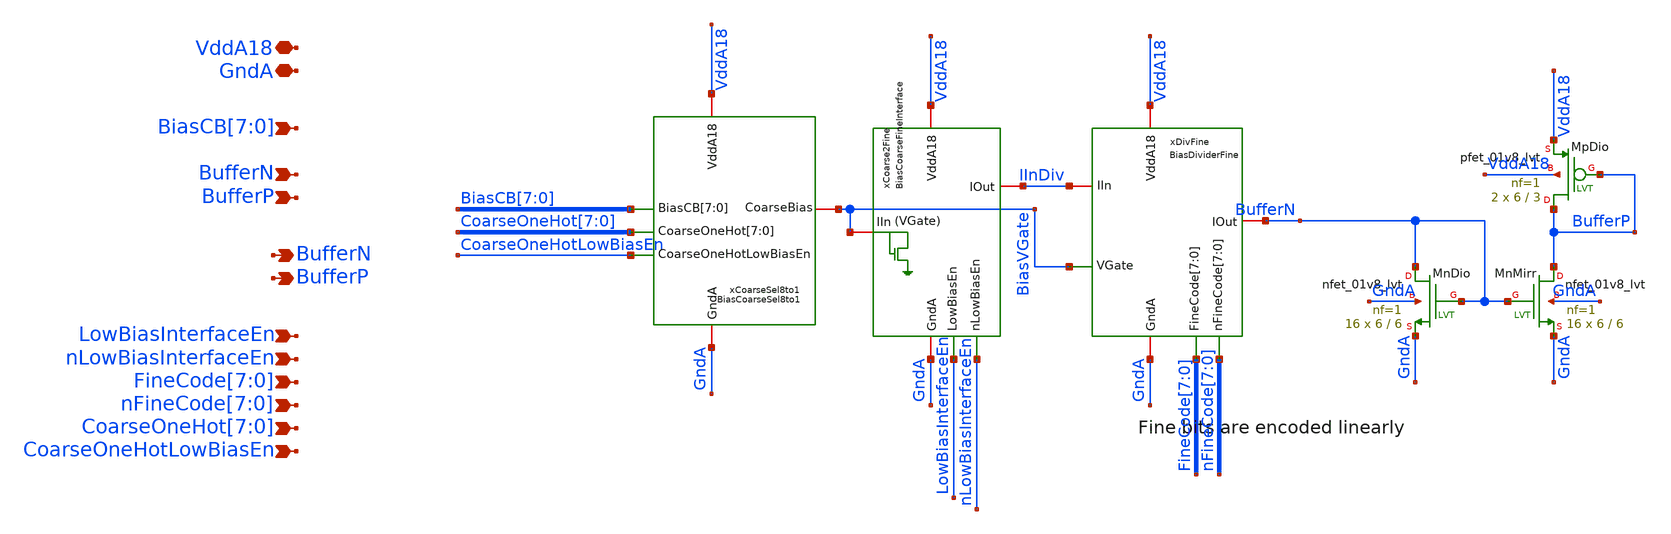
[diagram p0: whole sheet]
** sch_path: analog/klayout/production/final_merge_20260923/testbenches/cace/analog/xschem/BiasBranchBuffer.sch
**.subckt BiasBranchBuffer VddA18 GndA BufferN
*+ BiasCB[7],BiasCB[6],BiasCB[5],BiasCB[4],BiasCB[3],BiasCB[2],BiasCB[1],BiasCB[0] BufferN BufferP BufferP LowBiasInterfaceEn nLowBiasInterfaceEn
*+ FineCode[7],FineCode[6],FineCode[5],FineCode[4],FineCode[3],FineCode[2],FineCode[1],FineCode[0]
*+ nFineCode[7],nFineCode[6],nFineCode[5],nFineCode[4],nFineCode[3],nFineCode[2],nFineCode[1],nFineCode[0]
*+ CoarseOneHot[7],CoarseOneHot[6],CoarseOneHot[5],CoarseOneHot[4],CoarseOneHot[3],CoarseOneHot[2],CoarseOneHot[1],CoarseOneHot[0] CoarseOneHotLowBiasEn
*.iopin VddA18
*.iopin GndA
*.opin BufferN
*.ipin BiasCB[7],BiasCB[6],BiasCB[5],BiasCB[4],BiasCB[3],BiasCB[2],BiasCB[1],BiasCB[0]
*.ipin BufferN
*.ipin BufferP
*.opin BufferP
*.ipin LowBiasInterfaceEn
*.ipin nLowBiasInterfaceEn
*.ipin
*+ FineCode[7],FineCode[6],FineCode[5],FineCode[4],FineCode[3],FineCode[2],FineCode[1],FineCode[0]
*.ipin
*+ nFineCode[7],nFineCode[6],nFineCode[5],nFineCode[4],nFineCode[3],nFineCode[2],nFineCode[1],nFineCode[0]
*.ipin
*+ CoarseOneHot[7],CoarseOneHot[6],CoarseOneHot[5],CoarseOneHot[4],CoarseOneHot[3],CoarseOneHot[2],CoarseOneHot[1],CoarseOneHot[0]
*.ipin CoarseOneHotLowBiasEn
xCoarse2Fine VddA18 GndA LowBiasInterfaceEn nLowBiasInterfaceEn BiasVGate IInDiv
+ BiasCoarseFineInterface
xDivFine VddA18 GndA FineCode[7] FineCode[6] FineCode[5] FineCode[4] FineCode[3] FineCode[2]
+ FineCode[1] FineCode[0] nFineCode[7] nFineCode[6] nFineCode[5] nFineCode[4] nFineCode[3] nFineCode[2]
+ nFineCode[1] nFineCode[0] IInDiv BufferN BiasVGate BiasDividerFine
XMpDio BufferP BufferP VddA18 VddA18 sky130_fd_pr__pfet_01v8_lvt L=3 W=6 nf=1 ad='int((1 + 1)/2) * 6 / 1 * 0.29'
+ as='int((1 + 2)/2) * 6 / 1 * 0.29' pd='2*int((1 + 1)/2) * (6 / 1 + 0.29)' ps='2*int((1 + 2)/2) * (6 / 1 + 0.29)'
+ nrd='0.29 / 6 ' nrs='0.29 / 6 ' sa=0 sb=0 sd=0 mult=2 m=2
XMnDio BufferN BufferN GndA GndA sky130_fd_pr__nfet_01v8_lvt L=6 W=6 nf=1 ad='int((1 + 1)/2) * 6 / 1 * 0.29'
+ as='int((1 + 2)/2) * 6 / 1 * 0.29' pd='2*int((1 + 1)/2) * (6 / 1 + 0.29)' ps='2*int((1 + 2)/2) * (6 / 1 + 0.29)'
+ nrd='0.29 / 6 ' nrs='0.29 / 6 ' sa=0 sb=0 sd=0 mult=16 m=16
XMnMirr BufferP BufferN GndA GndA sky130_fd_pr__nfet_01v8_lvt L=6 W=6 nf=1 ad='int((1 + 1)/2) * 6 / 1 * 0.29'
+ as='int((1 + 2)/2) * 6 / 1 * 0.29' pd='2*int((1 + 1)/2) * (6 / 1 + 0.29)' ps='2*int((1 + 2)/2) * (6 / 1 + 0.29)'
+ nrd='0.29 / 6 ' nrs='0.29 / 6 ' sa=0 sb=0 sd=0 mult=16 m=16
xCoarseSel8to1 VddA18 GndA CoarseOneHot[7] CoarseOneHot[6] CoarseOneHot[5] CoarseOneHot[4]
+ CoarseOneHot[3] CoarseOneHot[2] CoarseOneHot[1] CoarseOneHot[0] CoarseOneHotLowBiasEn BiasCB[7] BiasCB[6] BiasCB[5]
+ BiasCB[4] BiasCB[3] BiasCB[2] BiasCB[1] BiasCB[0] BiasVGate BiasCoarseSel8to1
**.ends

* expanding   symbol:  BiasCoarseFineInterface.sym # of pins=6
** sym_path: analog/xschem/BiasCoarseFineInterface.sym
** sch_path: analog/xschem/BiasCoarseFineInterface.sch
.subckt BiasCoarseFineInterface VddA18 GndA LowBiasEn nLowBiasEn IIn IOut
*.iopin GndA
*.iopin VddA18
*.iopin IIn
*.iopin IOut
*.ipin nLowBiasEn
*.ipin LowBiasEn
XMpDisableHighBias HighBiasDioGate nLowBiasEn VddA18 VddA18 sky130_fd_pr__pfet_01v8 L=0.15 W=0.55 nf=1
+ ad='int((1 + 1)/2) * 0.55 / 1 * 0.29' as='int((1 + 2)/2) * 0.55 / 1 * 0.29' pd='2*int((1 + 1)/2) * (0.55 / 1 + 0.29)'
+ ps='2*int((1 + 2)/2) * (0.55 / 1 + 0.29)' nrd='0.29 / 0.55 ' nrs='0.29 / 0.55 ' sa=0 sb=0 sd=0 mult=1
+ m=1
XMpDioHighBias HighBiasDioDrain HighBiasDioGate VddA18 VddA18 sky130_fd_pr__pfet_01v8 L=0.5 W=64 nf=2
+ ad='int((2 + 1)/2) * 64 / 2 * 0.29' as='int((2 + 2)/2) * 64 / 2 * 0.29' pd='2*int((2 + 1)/2) * (64 / 2 + 0.29)'
+ ps='2*int((2 + 2)/2) * (64 / 2 + 0.29)' nrd='0.29 / 64 ' nrs='0.29 / 64 ' sa=0 sb=0 sd=0 mult=8 m=8
XMpMirrHighBias HighBiasMirr HighBiasDioGate VddA18 VddA18 sky130_fd_pr__pfet_01v8 L=0.5 W=64 nf=2 ad='int((2 + 1)/2) * 64 / 2 * 0.29'
+ as='int((2 + 2)/2) * 64 / 2 * 0.29' pd='2*int((2 + 1)/2) * (64 / 2 + 0.29)' ps='2*int((2 + 2)/2) * (64 / 2 + 0.29)'
+ nrd='0.29 / 64 ' nrs='0.29 / 64 ' sa=0 sb=0 sd=0 mult=8 m=8
XMpswDioHighBias HighBiasDioGate LowBiasEn HighBiasDioDrain VddA18 sky130_fd_pr__pfet_01v8 L=0.5 W=0.55
+ nf=1 ad='int((1 + 1)/2) * 0.55 / 1 * 0.29' as='int((1 + 2)/2) * 0.55 / 1 * 0.29' pd='2*int((1 + 1)/2) * (0.55 / 1 + 0.29)'
+ ps='2*int((1 + 2)/2) * (0.55 / 1 + 0.29)' nrd='0.29 / 0.55 ' nrs='0.29 / 0.55 ' sa=0 sb=0 sd=0 mult=1
+ m=1
XMnDisableDioHighBias HighBiasDioDrain LowBiasEn GndA GndA sky130_fd_pr__nfet_01v8 L=0.15 W=0.42 nf=1
+ ad='int((1 + 1)/2) * 0.42 / 1 * 0.29' as='int((1 + 2)/2) * 0.42 / 1 * 0.29' pd='2*int((1 + 1)/2) * (0.42 / 1 + 0.29)'
+ ps='2*int((1 + 2)/2) * (0.42 / 1 + 0.29)' nrd='0.29 / 0.42 ' nrs='0.29 / 0.42 ' sa=0 sb=0 sd=0 mult=1
+ m=1
XMpSelDioHighBias net1 LowBiasEn HighBiasDioDrain VddA18 sky130_fd_pr__pfet_01v8_hvt L=0.5 W=32 nf=2
+ ad='int((2 + 1)/2) * 32 / 2 * 0.29' as='int((2 + 2)/2) * 32 / 2 * 0.29' pd='2*int((2 + 1)/2) * (32 / 2 + 0.29)'
+ ps='2*int((2 + 2)/2) * (32 / 2 + 0.29)' nrd='0.29 / 32 ' nrs='0.29 / 32 ' sa=0 sb=0 sd=0 mult=8 m=8
XMpSelMirrHighBias IOut LowBiasEn HighBiasMirr VddA18 sky130_fd_pr__pfet_01v8_hvt L=0.5 W=32 nf=2 ad='int((2 + 1)/2) * 32 / 2 * 0.29'
+ as='int((2 + 2)/2) * 32 / 2 * 0.29' pd='2*int((2 + 1)/2) * (32 / 2 + 0.29)' ps='2*int((2 + 2)/2) * (32 / 2 + 0.29)'
+ nrd='0.29 / 32 ' nrs='0.29 / 32 ' sa=0 sb=0 sd=0 mult=8 m=8
XMnDisableOutMirr HighBiasMirr LowBiasEn GndA GndA sky130_fd_pr__nfet_01v8 L=0.15 W=0.42 nf=1 ad='int((1 + 1)/2) * 0.42 / 1 * 0.29'
+ as='int((1 + 2)/2) * 0.42 / 1 * 0.29' pd='2*int((1 + 1)/2) * (0.42 / 1 + 0.29)' ps='2*int((1 + 2)/2) * (0.42 / 1 + 0.29)'
+ nrd='0.29 / 0.42 ' nrs='0.29 / 0.42 ' sa=0 sb=0 sd=0 mult=1 m=1
XMpInDio IIn IIn net1 VddA18 sky130_fd_pr__pfet_01v8_lvt L=1 W=9 nf=1 ad='int((1 + 1)/2) * 9 / 1 * 0.29'
+ as='int((1 + 2)/2) * 9 / 1 * 0.29' pd='2*int((1 + 1)/2) * (9 / 1 + 0.29)' ps='2*int((1 + 2)/2) * (9 / 1 + 0.29)'
+ nrd='0.29 / 9 ' nrs='0.29 / 9 ' sa=0 sb=0 sd=0 mult=2 m=2
XMpDioLowBias1 LowBiasDioInt LowBiasDioGate VddA18 VddA18 sky130_fd_pr__pfet_01v8 L=2 W=4 nf=1 ad='int((1 + 1)/2) * 4 / 1 * 0.29'
+ as='int((1 + 2)/2) * 4 / 1 * 0.29' pd='2*int((1 + 1)/2) * (4 / 1 + 0.29)' ps='2*int((1 + 2)/2) * (4 / 1 + 0.29)'
+ nrd='0.29 / 4 ' nrs='0.29 / 4 ' sa=0 sb=0 sd=0 mult=2 m=2
XMpMirrLowBias1 LowBiasMirrInt LowBiasDioGate VddA18 VddA18 sky130_fd_pr__pfet_01v8 L=2 W=4 nf=1 ad='int((1 + 1)/2) * 4 / 1 * 0.29'
+ as='int((1 + 2)/2) * 4 / 1 * 0.29' pd='2*int((1 + 1)/2) * (4 / 1 + 0.29)' ps='2*int((1 + 2)/2) * (4 / 1 + 0.29)'
+ nrd='0.29 / 4 ' nrs='0.29 / 4 ' sa=0 sb=0 sd=0 mult=2 m=2
XMpDioLowBias2 LowBiasDioGate LowBiasDioGate LowBiasDioInt VddA18 sky130_fd_pr__pfet_01v8 L=2 W=4 nf=1
+ ad='int((1 + 1)/2) * 4 / 1 * 0.29' as='int((1 + 2)/2) * 4 / 1 * 0.29' pd='2*int((1 + 1)/2) * (4 / 1 + 0.29)'
+ ps='2*int((1 + 2)/2) * (4 / 1 + 0.29)' nrd='0.29 / 4 ' nrs='0.29 / 4 ' sa=0 sb=0 sd=0 mult=2 m=2
XMpMirrLowBias2 LowBiasMirr LowBiasDioGate LowBiasMirrInt VddA18 sky130_fd_pr__pfet_01v8 L=2 W=4 nf=1
+ ad='int((1 + 1)/2) * 4 / 1 * 0.29' as='int((1 + 2)/2) * 4 / 1 * 0.29' pd='2*int((1 + 1)/2) * (4 / 1 + 0.29)'
+ ps='2*int((1 + 2)/2) * (4 / 1 + 0.29)' nrd='0.29 / 4 ' nrs='0.29 / 4 ' sa=0 sb=0 sd=0 mult=2 m=2
XMpSelDioLowBias net1 nLowBiasEn LowBiasDioGate VddA18 sky130_fd_pr__pfet_01v8_lvt L=2 W=4 nf=1 ad='int((1 + 1)/2) * 4 / 1 * 0.29'
+ as='int((1 + 2)/2) * 4 / 1 * 0.29' pd='2*int((1 + 1)/2) * (4 / 1 + 0.29)' ps='2*int((1 + 2)/2) * (4 / 1 + 0.29)'
+ nrd='0.29 / 4 ' nrs='0.29 / 4 ' sa=0 sb=0 sd=0 mult=2 m=2
XMpSelMirrLowBias IOut nLowBiasEn LowBiasMirr VddA18 sky130_fd_pr__pfet_01v8_lvt L=2 W=4 nf=1 ad='int((1 + 1)/2) * 4 / 1 * 0.29'
+ as='int((1 + 2)/2) * 4 / 1 * 0.29' pd='2*int((1 + 1)/2) * (4 / 1 + 0.29)' ps='2*int((1 + 2)/2) * (4 / 1 + 0.29)'
+ nrd='0.29 / 4 ' nrs='0.29 / 4 ' sa=0 sb=0 sd=0 mult=2 m=2
.ends


* expanding   symbol:  BiasDividerFine.sym # of pins=7
** sym_path: analog/klayout/production/final_merge_20260923/testbenches/cace/analog/xschem/BiasDividerFine.sym
** sch_path: analog/klayout/production/final_merge_20260923/testbenches/cace/analog/xschem/BiasDividerFine.sch
.subckt BiasDividerFine VddA18 GndA FineCode[7] FineCode[6] FineCode[5] FineCode[4] FineCode[3]
+ FineCode[2] FineCode[1] FineCode[0] nFineCode[7] nFineCode[6] nFineCode[5] nFineCode[4] nFineCode[3]
+ nFineCode[2] nFineCode[1] nFineCode[0] IIn IOut VGate
*.iopin VddA18
*.iopin GndA
*.iopin IOut
*.ipin
*+ FineCode[7],FineCode[6],FineCode[5],FineCode[4],FineCode[3],FineCode[2],FineCode[1],FineCode[0]
*.ipin VGate
*.iopin IIn
*.ipin
*+ nFineCode[7],nFineCode[6],nFineCode[5],nFineCode[4],nFineCode[3],nFineCode[2],nFineCode[1],nFineCode[0]
xdiv0 Idiv1 Idiv0 VGate IOut VddA18 termDio nFineCode[0] FineCode[0] BiasDividerFineCell
xdiv1 Idiv2 Idiv1 VGate IOut VddA18 termDio nFineCode[1] FineCode[1] BiasDividerFineCell
xdiv2 Idiv3 Idiv2 VGate IOut VddA18 termDio nFineCode[2] FineCode[2] BiasDividerFineCell
xdiv3 Idiv4 Idiv3 VGate IOut VddA18 termDio nFineCode[3] FineCode[3] BiasDividerFineCell
xdiv4 Idiv5 Idiv4 VGate IOut VddA18 termDio nFineCode[4] FineCode[4] BiasDividerFineCell
xdiv5 Idiv6 Idiv5 VGate IOut VddA18 termDio nFineCode[5] FineCode[5] BiasDividerFineCell
xdiv6 Idiv7 Idiv6 VGate IOut VddA18 termDio nFineCode[6] FineCode[6] BiasDividerFineCell
xdiv7 IIn Idiv7 VGate IOut VddA18 termDio nFineCode[7] FineCode[7] BiasDividerFineCell
XMrTerm termDio VGate Idiv0 VddA18 sky130_fd_pr__pfet_01v8_lvt L=1 W=9 nf=1 ad='int((1 + 1)/2) * 9 / 1 * 0.29'
+ as='int((1 + 2)/2) * 9 / 1 * 0.29' pd='2*int((1 + 1)/2) * (9 / 1 + 0.29)' ps='2*int((1 + 2)/2) * (9 / 1 + 0.29)'
+ nrd='0.29 / 9 ' nrs='0.29 / 9 ' sa=0 sb=0 sd=0 mult=2 m=2
XMnterm termDio termDio GndA GndA sky130_fd_pr__nfet_01v8_lvt L=0.8 W=8 nf=1 ad='int((1 + 1)/2) * 8 / 1 * 0.29'
+ as='int((1 + 2)/2) * 8 / 1 * 0.29' pd='2*int((1 + 1)/2) * (8 / 1 + 0.29)' ps='2*int((1 + 2)/2) * (8 / 1 + 0.29)'
+ nrd='0.29 / 8 ' nrs='0.29 / 8 ' sa=0 sb=0 sd=0 mult=1 m=1
.ends


* expanding   symbol:  BiasCoarseSel8to1.sym # of pins=6
** sym_path: analog/xschem/BiasCoarseSel8to1.sym
** sch_path: analog/xschem/BiasCoarseSel8to1.sch
.subckt BiasCoarseSel8to1 VddA18 GndA CoarseOneHot[7] CoarseOneHot[6] CoarseOneHot[5]
+ CoarseOneHot[4] CoarseOneHot[3] CoarseOneHot[2] CoarseOneHot[1] CoarseOneHot[0] CoarseOneHotLowBiasEn BiasCB[7]
+ BiasCB[6] BiasCB[5] BiasCB[4] BiasCB[3] BiasCB[2] BiasCB[1] BiasCB[0] CoarseBias
*.ipin BiasCB[7],BiasCB[6],BiasCB[5],BiasCB[4],BiasCB[3],BiasCB[2],BiasCB[1],BiasCB[0]
*.ipin
*+ CoarseOneHot[7],CoarseOneHot[6],CoarseOneHot[5],CoarseOneHot[4],CoarseOneHot[3],CoarseOneHot[2],CoarseOneHot[1],CoarseOneHot[0]
*.iopin CoarseBias
*.iopin VddA18
*.iopin GndA
*.ipin CoarseOneHotLowBiasEn
XMpswB0 net1 CoarseOneHot[0] VddA18 VddA18 sky130_fd_pr__pfet_01v8 L=0.15 W=0.55 nf=1 ad='int((1 + 1)/2) * 0.55 / 1 * 0.29'
+ as='int((1 + 2)/2) * 0.55 / 1 * 0.29' pd='2*int((1 + 1)/2) * (0.55 / 1 + 0.29)' ps='2*int((1 + 2)/2) * (0.55 / 1 + 0.29)'
+ nrd='0.29 / 0.55 ' nrs='0.29 / 0.55 ' sa=0 sb=0 sd=0 mult=1 m=1
XMnswuB0 CoarseBias CoarseOneHot[0] net1 GndA sky130_fd_pr__nfet_01v8 L=0.15 W=1 nf=1 ad='int((1 + 1)/2) * 1 / 1 * 0.29'
+ as='int((1 + 2)/2) * 1 / 1 * 0.29' pd='2*int((1 + 1)/2) * (1 / 1 + 0.29)' ps='2*int((1 + 2)/2) * (1 / 1 + 0.29)'
+ nrd='0.29 / 1 ' nrs='0.29 / 1 ' sa=0 sb=0 sd=0 mult=1 m=1
XMnswlB0 net1 CoarseOneHot[0] MirrB0_drain GndA sky130_fd_pr__nfet_01v8_lvt L=0.15 W=1 nf=1 ad='int((1 + 1)/2) * 1 / 1 * 0.29'
+ as='int((1 + 2)/2) * 1 / 1 * 0.29' pd='2*int((1 + 1)/2) * (1 / 1 + 0.29)' ps='2*int((1 + 2)/2) * (1 / 1 + 0.29)'
+ nrd='0.29 / 1 ' nrs='0.29 / 1 ' sa=0 sb=0 sd=0 mult=1 m=1
XMmirrB0 MirrB0_drain BiasCB[0] GndA GndA sky130_fd_pr__nfet_01v8_lvt L=5 W=1.8 nf=1 ad='int((1 + 1)/2) * 1.8 / 1 * 0.29'
+ as='int((1 + 2)/2) * 1.8 / 1 * 0.29' pd='2*int((1 + 1)/2) * (1.8 / 1 + 0.29)' ps='2*int((1 + 2)/2) * (1.8 / 1 + 0.29)'
+ nrd='0.29 / 1.8 ' nrs='0.29 / 1.8 ' sa=0 sb=0 sd=0 mult=8 m=8
XMpswB1 net2 CoarseOneHot[1] VddA18 VddA18 sky130_fd_pr__pfet_01v8 L=0.15 W=0.55 nf=1 ad='int((1 + 1)/2) * 0.55 / 1 * 0.29'
+ as='int((1 + 2)/2) * 0.55 / 1 * 0.29' pd='2*int((1 + 1)/2) * (0.55 / 1 + 0.29)' ps='2*int((1 + 2)/2) * (0.55 / 1 + 0.29)'
+ nrd='0.29 / 0.55 ' nrs='0.29 / 0.55 ' sa=0 sb=0 sd=0 mult=1 m=1
XMnswuB1 CoarseBias CoarseOneHot[1] net2 GndA sky130_fd_pr__nfet_01v8 L=1 W=1 nf=1 ad='int((1 + 1)/2) * 1 / 1 * 0.29'
+ as='int((1 + 2)/2) * 1 / 1 * 0.29' pd='2*int((1 + 1)/2) * (1 / 1 + 0.29)' ps='2*int((1 + 2)/2) * (1 / 1 + 0.29)'
+ nrd='0.29 / 1 ' nrs='0.29 / 1 ' sa=0 sb=0 sd=0 mult=1 m=1
XMnswlB1 net2 CoarseOneHot[1] MirrB1_drain GndA sky130_fd_pr__nfet_01v8 L=1 W=1 nf=1 ad='int((1 + 1)/2) * 1 / 1 * 0.29'
+ as='int((1 + 2)/2) * 1 / 1 * 0.29' pd='2*int((1 + 1)/2) * (1 / 1 + 0.29)' ps='2*int((1 + 2)/2) * (1 / 1 + 0.29)'
+ nrd='0.29 / 1 ' nrs='0.29 / 1 ' sa=0 sb=0 sd=0 mult=1 m=1
XMmirrB1 MirrB1_drain BiasCB[1] GndA GndA sky130_fd_pr__nfet_01v8_lvt L=9.98 W=0.98 nf=1 ad='int((1 + 1)/2) * 0.98 / 1 * 0.29'
+ as='int((1 + 2)/2) * 0.98 / 1 * 0.29' pd='2*int((1 + 1)/2) * (0.98 / 1 + 0.29)' ps='2*int((1 + 2)/2) * (0.98 / 1 + 0.29)'
+ nrd='0.29 / 0.98 ' nrs='0.29 / 0.98 ' sa=0 sb=0 sd=0 mult=8 m=8
XMpswB2 net3 CoarseOneHot[2] VddA18 VddA18 sky130_fd_pr__pfet_01v8 L=0.15 W=0.55 nf=1 ad='int((1 + 1)/2) * 0.55 / 1 * 0.29'
+ as='int((1 + 2)/2) * 0.55 / 1 * 0.29' pd='2*int((1 + 1)/2) * (0.55 / 1 + 0.29)' ps='2*int((1 + 2)/2) * (0.55 / 1 + 0.29)'
+ nrd='0.29 / 0.55 ' nrs='0.29 / 0.55 ' sa=0 sb=0 sd=0 mult=1 m=1
XMnswuB2 CoarseBias CoarseOneHot[2] net3 GndA sky130_fd_pr__nfet_01v8 L=1 W=1 nf=1 ad='int((1 + 1)/2) * 1 / 1 * 0.29'
+ as='int((1 + 2)/2) * 1 / 1 * 0.29' pd='2*int((1 + 1)/2) * (1 / 1 + 0.29)' ps='2*int((1 + 2)/2) * (1 / 1 + 0.29)'
+ nrd='0.29 / 1 ' nrs='0.29 / 1 ' sa=0 sb=0 sd=0 mult=1 m=1
XMnswlB2 net3 CoarseOneHot[2] MirrB2_drain GndA sky130_fd_pr__nfet_01v8 L=1 W=1 nf=1 ad='int((1 + 1)/2) * 1 / 1 * 0.29'
+ as='int((1 + 2)/2) * 1 / 1 * 0.29' pd='2*int((1 + 1)/2) * (1 / 1 + 0.29)' ps='2*int((1 + 2)/2) * (1 / 1 + 0.29)'
+ nrd='0.29 / 1 ' nrs='0.29 / 1 ' sa=0 sb=0 sd=0 mult=1 m=1
XMmirrhB2 MirrB2_drain BiasCB[2] net4 GndA sky130_fd_pr__nfet_01v8_lvt L=5 W=1.98 nf=1 ad='int((1 + 1)/2) * 1.98 / 1 * 0.29'
+ as='int((1 + 2)/2) * 1.98 / 1 * 0.29' pd='2*int((1 + 1)/2) * (1.98 / 1 + 0.29)' ps='2*int((1 + 2)/2) * (1.98 / 1 + 0.29)'
+ nrd='0.29 / 1.98 ' nrs='0.29 / 1.98 ' sa=0 sb=0 sd=0 mult=1 m=1
XMmirrgB2 net4 BiasCB[2] net5 GndA sky130_fd_pr__nfet_01v8_lvt L=5 W=1.98 nf=1 ad='int((1 + 1)/2) * 1.98 / 1 * 0.29'
+ as='int((1 + 2)/2) * 1.98 / 1 * 0.29' pd='2*int((1 + 1)/2) * (1.98 / 1 + 0.29)' ps='2*int((1 + 2)/2) * (1.98 / 1 + 0.29)'
+ nrd='0.29 / 1.98 ' nrs='0.29 / 1.98 ' sa=0 sb=0 sd=0 mult=1 m=1
XMmirrfB2 net5 BiasCB[2] net6 GndA sky130_fd_pr__nfet_01v8_lvt L=5 W=1.98 nf=1 ad='int((1 + 1)/2) * 1.98 / 1 * 0.29'
+ as='int((1 + 2)/2) * 1.98 / 1 * 0.29' pd='2*int((1 + 1)/2) * (1.98 / 1 + 0.29)' ps='2*int((1 + 2)/2) * (1.98 / 1 + 0.29)'
+ nrd='0.29 / 1.98 ' nrs='0.29 / 1.98 ' sa=0 sb=0 sd=0 mult=1 m=1
XMmirrfB1 net6 BiasCB[2] net7 GndA sky130_fd_pr__nfet_01v8_lvt L=5 W=1.98 nf=1 ad='int((1 + 1)/2) * 1.98 / 1 * 0.29'
+ as='int((1 + 2)/2) * 1.98 / 1 * 0.29' pd='2*int((1 + 1)/2) * (1.98 / 1 + 0.29)' ps='2*int((1 + 2)/2) * (1.98 / 1 + 0.29)'
+ nrd='0.29 / 1.98 ' nrs='0.29 / 1.98 ' sa=0 sb=0 sd=0 mult=1 m=1
XMmirreB2 net7 BiasCB[2] net8 GndA sky130_fd_pr__nfet_01v8_lvt L=5 W=1.98 nf=1 ad='int((1 + 1)/2) * 1.98 / 1 * 0.29'
+ as='int((1 + 2)/2) * 1.98 / 1 * 0.29' pd='2*int((1 + 1)/2) * (1.98 / 1 + 0.29)' ps='2*int((1 + 2)/2) * (1.98 / 1 + 0.29)'
+ nrd='0.29 / 1.98 ' nrs='0.29 / 1.98 ' sa=0 sb=0 sd=0 mult=1 m=1
XMmirrcB2 net8 BiasCB[2] net9 GndA sky130_fd_pr__nfet_01v8_lvt L=5 W=1.98 nf=1 ad='int((1 + 1)/2) * 1.98 / 1 * 0.29'
+ as='int((1 + 2)/2) * 1.98 / 1 * 0.29' pd='2*int((1 + 1)/2) * (1.98 / 1 + 0.29)' ps='2*int((1 + 2)/2) * (1.98 / 1 + 0.29)'
+ nrd='0.29 / 1.98 ' nrs='0.29 / 1.98 ' sa=0 sb=0 sd=0 mult=1 m=1
XMmirrbB2 net9 BiasCB[2] net10 GndA sky130_fd_pr__nfet_01v8_lvt L=5 W=1.98 nf=1 ad='int((1 + 1)/2) * 1.98 / 1 * 0.29'
+ as='int((1 + 2)/2) * 1.98 / 1 * 0.29' pd='2*int((1 + 1)/2) * (1.98 / 1 + 0.29)' ps='2*int((1 + 2)/2) * (1.98 / 1 + 0.29)'
+ nrd='0.29 / 1.98 ' nrs='0.29 / 1.98 ' sa=0 sb=0 sd=0 mult=1 m=1
XMmirraB2 net10 BiasCB[2] GndA GndA sky130_fd_pr__nfet_01v8_lvt L=5 W=1.98 nf=1 ad='int((1 + 1)/2) * 1.98 / 1 * 0.29'
+ as='int((1 + 2)/2) * 1.98 / 1 * 0.29' pd='2*int((1 + 1)/2) * (1.98 / 1 + 0.29)' ps='2*int((1 + 2)/2) * (1.98 / 1 + 0.29)'
+ nrd='0.29 / 1.98 ' nrs='0.29 / 1.98 ' sa=0 sb=0 sd=0 mult=1 m=1
XMpswB3 net11 CoarseOneHot[3] VddA18 VddA18 sky130_fd_pr__pfet_01v8 L=0.15 W=0.55 nf=1 ad='int((1 + 1)/2) * 0.55 / 1 * 0.29'
+ as='int((1 + 2)/2) * 0.55 / 1 * 0.29' pd='2*int((1 + 1)/2) * (0.55 / 1 + 0.29)' ps='2*int((1 + 2)/2) * (0.55 / 1 + 0.29)'
+ nrd='0.29 / 0.55 ' nrs='0.29 / 0.55 ' sa=0 sb=0 sd=0 mult=1 m=1
XMnswuB3 CoarseBias CoarseOneHot[3] net11 GndA sky130_fd_pr__nfet_01v8 L=1 W=1 nf=1 ad='int((1 + 1)/2) * 1 / 1 * 0.29'
+ as='int((1 + 2)/2) * 1 / 1 * 0.29' pd='2*int((1 + 1)/2) * (1 / 1 + 0.29)' ps='2*int((1 + 2)/2) * (1 / 1 + 0.29)'
+ nrd='0.29 / 1 ' nrs='0.29 / 1 ' sa=0 sb=0 sd=0 mult=1 m=1
XMnswlB3 net11 CoarseOneHot[3] MirrB3_drain GndA sky130_fd_pr__nfet_01v8 L=1 W=1 nf=1 ad='int((1 + 1)/2) * 1 / 1 * 0.29'
+ as='int((1 + 2)/2) * 1 / 1 * 0.29' pd='2*int((1 + 1)/2) * (1 / 1 + 0.29)' ps='2*int((1 + 2)/2) * (1 / 1 + 0.29)'
+ nrd='0.29 / 1 ' nrs='0.29 / 1 ' sa=0 sb=0 sd=0 mult=1 m=1
XMmirrhB3 MirrB3_drain BiasCB[3] net12 GndA sky130_fd_pr__nfet_01v8_lvt L=9.98 W=0.98 nf=1 ad='int((1 + 1)/2) * 0.98 / 1 * 0.29'
+ as='int((1 + 2)/2) * 0.98 / 1 * 0.29' pd='2*int((1 + 1)/2) * (0.98 / 1 + 0.29)' ps='2*int((1 + 2)/2) * (0.98 / 1 + 0.29)'
+ nrd='0.29 / 0.98 ' nrs='0.29 / 0.98 ' sa=0 sb=0 sd=0 mult=1 m=1
XMmirrgB3 net12 BiasCB[3] net13 GndA sky130_fd_pr__nfet_01v8_lvt L=9.98 W=0.98 nf=1 ad='int((1 + 1)/2) * 0.98 / 1 * 0.29'
+ as='int((1 + 2)/2) * 0.98 / 1 * 0.29' pd='2*int((1 + 1)/2) * (0.98 / 1 + 0.29)' ps='2*int((1 + 2)/2) * (0.98 / 1 + 0.29)'
+ nrd='0.29 / 0.98 ' nrs='0.29 / 0.98 ' sa=0 sb=0 sd=0 mult=1 m=1
XMmirrfB3 net13 BiasCB[3] net14 GndA sky130_fd_pr__nfet_01v8_lvt L=9.98 W=0.98 nf=1 ad='int((1 + 1)/2) * 0.98 / 1 * 0.29'
+ as='int((1 + 2)/2) * 0.98 / 1 * 0.29' pd='2*int((1 + 1)/2) * (0.98 / 1 + 0.29)' ps='2*int((1 + 2)/2) * (0.98 / 1 + 0.29)'
+ nrd='0.29 / 0.98 ' nrs='0.29 / 0.98 ' sa=0 sb=0 sd=0 mult=1 m=1
XMmirreB3 net14 BiasCB[3] net15 GndA sky130_fd_pr__nfet_01v8_lvt L=9.98 W=0.98 nf=1 ad='int((1 + 1)/2) * 0.98 / 1 * 0.29'
+ as='int((1 + 2)/2) * 0.98 / 1 * 0.29' pd='2*int((1 + 1)/2) * (0.98 / 1 + 0.29)' ps='2*int((1 + 2)/2) * (0.98 / 1 + 0.29)'
+ nrd='0.29 / 0.98 ' nrs='0.29 / 0.98 ' sa=0 sb=0 sd=0 mult=1 m=1
XMmirrdB3 net15 BiasCB[3] net16 GndA sky130_fd_pr__nfet_01v8_lvt L=9.98 W=0.98 nf=1 ad='int((1 + 1)/2) * 0.98 / 1 * 0.29'
+ as='int((1 + 2)/2) * 0.98 / 1 * 0.29' pd='2*int((1 + 1)/2) * (0.98 / 1 + 0.29)' ps='2*int((1 + 2)/2) * (0.98 / 1 + 0.29)'
+ nrd='0.29 / 0.98 ' nrs='0.29 / 0.98 ' sa=0 sb=0 sd=0 mult=1 m=1
XMmirrcB3 net16 BiasCB[3] net17 GndA sky130_fd_pr__nfet_01v8_lvt L=9.98 W=0.98 nf=1 ad='int((1 + 1)/2) * 0.98 / 1 * 0.29'
+ as='int((1 + 2)/2) * 0.98 / 1 * 0.29' pd='2*int((1 + 1)/2) * (0.98 / 1 + 0.29)' ps='2*int((1 + 2)/2) * (0.98 / 1 + 0.29)'
+ nrd='0.29 / 0.98 ' nrs='0.29 / 0.98 ' sa=0 sb=0 sd=0 mult=1 m=1
XMmirrbB3 net17 BiasCB[3] net18 GndA sky130_fd_pr__nfet_01v8_lvt L=9.98 W=0.98 nf=1 ad='int((1 + 1)/2) * 0.98 / 1 * 0.29'
+ as='int((1 + 2)/2) * 0.98 / 1 * 0.29' pd='2*int((1 + 1)/2) * (0.98 / 1 + 0.29)' ps='2*int((1 + 2)/2) * (0.98 / 1 + 0.29)'
+ nrd='0.29 / 0.98 ' nrs='0.29 / 0.98 ' sa=0 sb=0 sd=0 mult=1 m=1
XMmirraB3 net18 BiasCB[3] GndA GndA sky130_fd_pr__nfet_01v8_lvt L=9.98 W=0.98 nf=1 ad='int((1 + 1)/2) * 0.98 / 1 * 0.29'
+ as='int((1 + 2)/2) * 0.98 / 1 * 0.29' pd='2*int((1 + 1)/2) * (0.98 / 1 + 0.29)' ps='2*int((1 + 2)/2) * (0.98 / 1 + 0.29)'
+ nrd='0.29 / 0.98 ' nrs='0.29 / 0.98 ' sa=0 sb=0 sd=0 mult=1 m=1
XMnswuB4to7 CoarseBias CoarseOneHotLowBiasEn MirrB4o5o6o7_drain GndA sky130_fd_pr__nfet_01v8 L=1 W=1
+ nf=1 ad='int((1 + 1)/2) * 1 / 1 * 0.29' as='int((1 + 2)/2) * 1 / 1 * 0.29' pd='2*int((1 + 1)/2) * (1 / 1 + 0.29)'
+ ps='2*int((1 + 2)/2) * (1 / 1 + 0.29)' nrd='0.29 / 1 ' nrs='0.29 / 1 ' sa=0 sb=0 sd=0 mult=1 m=1
XMmirrhB4to7 MirrB4o5o6o7_drain MirrB4o5o6o7_gate net19 GndA sky130_fd_pr__nfet_01v8_lvt L=20 W=0.5 nf=1
+ ad='int((1 + 1)/2) * 0.5 / 1 * 0.29' as='int((1 + 2)/2) * 0.5 / 1 * 0.29' pd='2*int((1 + 1)/2) * (0.5 / 1 + 0.29)'
+ ps='2*int((1 + 2)/2) * (0.5 / 1 + 0.29)' nrd='0.29 / 0.5 ' nrs='0.29 / 0.5 ' sa=0 sb=0 sd=0 mult=1 m=1
XMmirraB4to7 net25 MirrB4o5o6o7_gate GndA GndA sky130_fd_pr__nfet_01v8_lvt L=20 W=0.5 nf=1 ad='int((1 + 1)/2) * 0.5 / 1 * 0.29'
+ as='int((1 + 2)/2) * 0.5 / 1 * 0.29' pd='2*int((1 + 1)/2) * (0.5 / 1 + 0.29)' ps='2*int((1 + 2)/2) * (0.5 / 1 + 0.29)'
+ nrd='0.29 / 0.5 ' nrs='0.29 / 0.5 ' sa=0 sb=0 sd=0 mult=1 m=1
XMmirrbB4to7 net24 MirrB4o5o6o7_gate net25 GndA sky130_fd_pr__nfet_01v8_lvt L=20 W=0.5 nf=1 ad='int((1 + 1)/2) * 0.5 / 1 * 0.29'
+ as='int((1 + 2)/2) * 0.5 / 1 * 0.29' pd='2*int((1 + 1)/2) * (0.5 / 1 + 0.29)' ps='2*int((1 + 2)/2) * (0.5 / 1 + 0.29)'
+ nrd='0.29 / 0.5 ' nrs='0.29 / 0.5 ' sa=0 sb=0 sd=0 mult=1 m=1
XMmirrcB4to7 net23 MirrB4o5o6o7_gate net24 GndA sky130_fd_pr__nfet_01v8_lvt L=20 W=0.5 nf=1 ad='int((1 + 1)/2) * 0.5 / 1 * 0.29'
+ as='int((1 + 2)/2) * 0.5 / 1 * 0.29' pd='2*int((1 + 1)/2) * (0.5 / 1 + 0.29)' ps='2*int((1 + 2)/2) * (0.5 / 1 + 0.29)'
+ nrd='0.29 / 0.5 ' nrs='0.29 / 0.5 ' sa=0 sb=0 sd=0 mult=1 m=1
XMmirrdB4to7 net22 MirrB4o5o6o7_gate net23 GndA sky130_fd_pr__nfet_01v8_lvt L=20 W=0.5 nf=1 ad='int((1 + 1)/2) * 0.5 / 1 * 0.29'
+ as='int((1 + 2)/2) * 0.5 / 1 * 0.29' pd='2*int((1 + 1)/2) * (0.5 / 1 + 0.29)' ps='2*int((1 + 2)/2) * (0.5 / 1 + 0.29)'
+ nrd='0.29 / 0.5 ' nrs='0.29 / 0.5 ' sa=0 sb=0 sd=0 mult=1 m=1
XMmirreB4to7 net21 MirrB4o5o6o7_gate net22 GndA sky130_fd_pr__nfet_01v8_lvt L=20 W=0.5 nf=1 ad='int((1 + 1)/2) * 0.5 / 1 * 0.29'
+ as='int((1 + 2)/2) * 0.5 / 1 * 0.29' pd='2*int((1 + 1)/2) * (0.5 / 1 + 0.29)' ps='2*int((1 + 2)/2) * (0.5 / 1 + 0.29)'
+ nrd='0.29 / 0.5 ' nrs='0.29 / 0.5 ' sa=0 sb=0 sd=0 mult=1 m=1
XMmirrfB4to7 net20 MirrB4o5o6o7_gate net21 GndA sky130_fd_pr__nfet_01v8_lvt L=20 W=0.5 nf=1 ad='int((1 + 1)/2) * 0.5 / 1 * 0.29'
+ as='int((1 + 2)/2) * 0.5 / 1 * 0.29' pd='2*int((1 + 1)/2) * (0.5 / 1 + 0.29)' ps='2*int((1 + 2)/2) * (0.5 / 1 + 0.29)'
+ nrd='0.29 / 0.5 ' nrs='0.29 / 0.5 ' sa=0 sb=0 sd=0 mult=1 m=1
XMmirrgB4to7 net19 MirrB4o5o6o7_gate net20 GndA sky130_fd_pr__nfet_01v8_lvt L=20 W=0.5 nf=1 ad='int((1 + 1)/2) * 0.5 / 1 * 0.29'
+ as='int((1 + 2)/2) * 0.5 / 1 * 0.29' pd='2*int((1 + 1)/2) * (0.5 / 1 + 0.29)' ps='2*int((1 + 2)/2) * (0.5 / 1 + 0.29)'
+ nrd='0.29 / 0.5 ' nrs='0.29 / 0.5 ' sa=0 sb=0 sd=0 mult=1 m=1
XMnswl7 MirrB4o5o6o7_gate CoarseOneHot[7] BiasCB[7] GndA sky130_fd_pr__nfet_01v8 L=1 W=1 nf=1 ad='int((1 + 1)/2) * 1 / 1 * 0.29'
+ as='int((1 + 2)/2) * 1 / 1 * 0.29' pd='2*int((1 + 1)/2) * (1 / 1 + 0.29)' ps='2*int((1 + 2)/2) * (1 / 1 + 0.29)'
+ nrd='0.29 / 1 ' nrs='0.29 / 1 ' sa=0 sb=0 sd=0 mult=1 m=1
XMnswlB6 MirrB4o5o6o7_gate CoarseOneHot[6] BiasCB[6] GndA sky130_fd_pr__nfet_01v8 L=1 W=1 nf=1 ad='int((1 + 1)/2) * 1 / 1 * 0.29'
+ as='int((1 + 2)/2) * 1 / 1 * 0.29' pd='2*int((1 + 1)/2) * (1 / 1 + 0.29)' ps='2*int((1 + 2)/2) * (1 / 1 + 0.29)'
+ nrd='0.29 / 1 ' nrs='0.29 / 1 ' sa=0 sb=0 sd=0 mult=1 m=1
XMnswlB5 MirrB4o5o6o7_gate CoarseOneHot[5] BiasCB[5] GndA sky130_fd_pr__nfet_01v8 L=1 W=1 nf=1 ad='int((1 + 1)/2) * 1 / 1 * 0.29'
+ as='int((1 + 2)/2) * 1 / 1 * 0.29' pd='2*int((1 + 1)/2) * (1 / 1 + 0.29)' ps='2*int((1 + 2)/2) * (1 / 1 + 0.29)'
+ nrd='0.29 / 1 ' nrs='0.29 / 1 ' sa=0 sb=0 sd=0 mult=1 m=1
XMnswlB4 MirrB4o5o6o7_gate CoarseOneHot[4] BiasCB[4] GndA sky130_fd_pr__nfet_01v8 L=1 W=1 nf=1 ad='int((1 + 1)/2) * 1 / 1 * 0.29'
+ as='int((1 + 2)/2) * 1 / 1 * 0.29' pd='2*int((1 + 1)/2) * (1 / 1 + 0.29)' ps='2*int((1 + 2)/2) * (1 / 1 + 0.29)'
+ nrd='0.29 / 1 ' nrs='0.29 / 1 ' sa=0 sb=0 sd=0 mult=1 m=1
.ends


* expanding   symbol:  BiasDividerFineCell.sym # of pins=8
** sym_path: analog/xschem/BiasDividerFineCell.sym
** sch_path: analog/xschem/BiasDividerFineCell.sch
.subckt BiasDividerFineCell IPrev INext VGate IOut VddA18 INOut nSel Sel
*.iopin INext
*.iopin IOut
*.iopin IPrev
*.ipin VGate
*.iopin VddA18
*.ipin nSel
*.ipin Sel
*.iopin INOut
XMr INext VGate IPrev VddA18 sky130_fd_pr__pfet_01v8 L=1 W=9 nf=1 ad='int((1 + 1)/2) * 9 / 1 * 0.29'
+ as='int((1 + 2)/2) * 9 / 1 * 0.29' pd='2*int((1 + 1)/2) * (9 / 1 + 0.29)' ps='2*int((1 + 2)/2) * (9 / 1 + 0.29)'
+ nrd='0.29 / 9 ' nrs='0.29 / 9 ' sa=0 sb=0 sd=0 mult=2 m=2
XM2ru net1 VGate IPrev VddA18 sky130_fd_pr__pfet_01v8 L=1 W=9 nf=1 ad='int((1 + 1)/2) * 9 / 1 * 0.29'
+ as='int((1 + 2)/2) * 9 / 1 * 0.29' pd='2*int((1 + 1)/2) * (9 / 1 + 0.29)' ps='2*int((1 + 2)/2) * (9 / 1 + 0.29)'
+ nrd='0.29 / 9 ' nrs='0.29 / 9 ' sa=0 sb=0 sd=0 mult=2 m=2
XM2rl net2 VGate net1 VddA18 sky130_fd_pr__pfet_01v8 L=1 W=9 nf=1 ad='int((1 + 1)/2) * 9 / 1 * 0.29'
+ as='int((1 + 2)/2) * 9 / 1 * 0.29' pd='2*int((1 + 1)/2) * (9 / 1 + 0.29)' ps='2*int((1 + 2)/2) * (9 / 1 + 0.29)'
+ nrd='0.29 / 9 ' nrs='0.29 / 9 ' sa=0 sb=0 sd=0 mult=2 m=2
XMswNOut INOut Sel net2 VddA18 sky130_fd_pr__pfet_01v8 L=0.5 W=2 nf=1 ad='int((1 + 1)/2) * 2 / 1 * 0.29'
+ as='int((1 + 2)/2) * 2 / 1 * 0.29' pd='2*int((1 + 1)/2) * (2 / 1 + 0.29)' ps='2*int((1 + 2)/2) * (2 / 1 + 0.29)'
+ nrd='0.29 / 2 ' nrs='0.29 / 2 ' sa=0 sb=0 sd=0 mult=1 m=1
XMswOut IOut nSel net2 VddA18 sky130_fd_pr__pfet_01v8 L=0.5 W=2 nf=1 ad='int((1 + 1)/2) * 2 / 1 * 0.29'
+ as='int((1 + 2)/2) * 2 / 1 * 0.29' pd='2*int((1 + 1)/2) * (2 / 1 + 0.29)' ps='2*int((1 + 2)/2) * (2 / 1 + 0.29)'
+ nrd='0.29 / 2 ' nrs='0.29 / 2 ' sa=0 sb=0 sd=0 mult=1 m=1
.ends

.end
